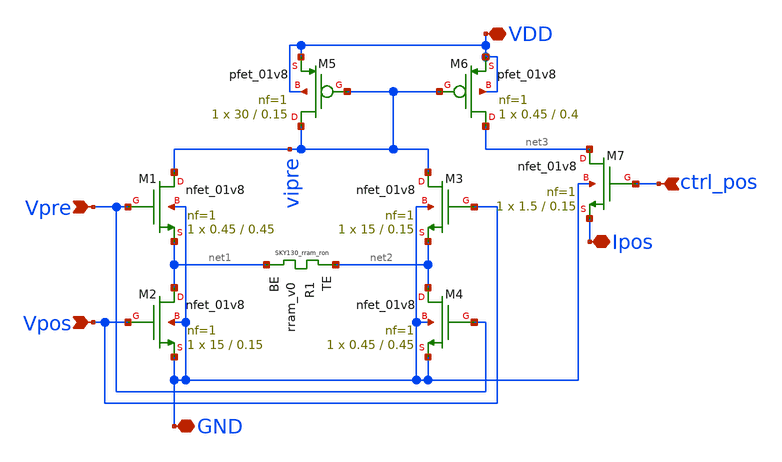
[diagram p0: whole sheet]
** sch_path: SNN/Syn_7T1R.sch
**.subckt Syn_7T1R Vpre Vpos GND Ipos VDD ctrl_pos
*.ipin Vpre
*.ipin Vpos
*.iopin GND
*.iopin Ipos
*.iopin VDD
*.ipin ctrl_pos
XM1 vipre Vpre net1 GND sky130_fd_pr__nfet_01v8 L=0.45 W=0.45 nf=1 ad='int((nf+1)/2) * W/nf * 0.29' as='int((nf+2)/2) * W/nf * 0.29'
+ pd='2*int((nf+1)/2) * (W/nf + 0.29)' ps='2*int((nf+2)/2) * (W/nf + 0.29)' nrd='0.29 / W' nrs='0.29 / W'
+ sa=0 sb=0 sd=0 mult=1 m=1
XR1 net2 net1 rram_v0
XM3 vipre Vpos net2 GND sky130_fd_pr__nfet_01v8 L=0.15 W=15 nf=1 ad='int((nf+1)/2) * W/nf * 0.29' as='int((nf+2)/2) * W/nf * 0.29'
+ pd='2*int((nf+1)/2) * (W/nf + 0.29)' ps='2*int((nf+2)/2) * (W/nf + 0.29)' nrd='0.29 / W' nrs='0.29 / W'
+ sa=0 sb=0 sd=0 mult=1 m=1
XM6 net3 vipre VDD VDD sky130_fd_pr__pfet_01v8 L=0.4 W=0.45 nf=1 ad='int((nf+1)/2) * W/nf * 0.29' as='int((nf+2)/2) * W/nf * 0.29'
+ pd='2*int((nf+1)/2) * (W/nf + 0.29)' ps='2*int((nf+2)/2) * (W/nf + 0.29)' nrd='0.29 / W' nrs='0.29 / W'
+ sa=0 sb=0 sd=0 mult=1 m=1
XM5 vipre vipre VDD VDD sky130_fd_pr__pfet_01v8 L=0.15 W=30 nf=1 ad='int((nf+1)/2) * W/nf * 0.29' as='int((nf+2)/2) * W/nf * 0.29'
+ pd='2*int((nf+1)/2) * (W/nf + 0.29)' ps='2*int((nf+2)/2) * (W/nf + 0.29)' nrd='0.29 / W' nrs='0.29 / W'
+ sa=0 sb=0 sd=0 mult=1 m=1
XM2 net1 Vpos GND GND sky130_fd_pr__nfet_01v8 L=0.15 W=15 nf=1 ad='int((nf+1)/2) * W/nf * 0.29' as='int((nf+2)/2) * W/nf * 0.29'
+ pd='2*int((nf+1)/2) * (W/nf + 0.29)' ps='2*int((nf+2)/2) * (W/nf + 0.29)' nrd='0.29 / W' nrs='0.29 / W'
+ sa=0 sb=0 sd=0 mult=1 m=1
XM4 net2 Vpre GND GND sky130_fd_pr__nfet_01v8 L=0.45 W=0.45 nf=1 ad='int((nf+1)/2) * W/nf * 0.29' as='int((nf+2)/2) * W/nf * 0.29'
+ pd='2*int((nf+1)/2) * (W/nf + 0.29)' ps='2*int((nf+2)/2) * (W/nf + 0.29)' nrd='0.29 / W' nrs='0.29 / W'
+ sa=0 sb=0 sd=0 mult=1 m=1
XM7 net3 ctrl_pos Ipos GND sky130_fd_pr__nfet_01v8 L=0.15 W=1.5 nf=1 ad='int((nf+1)/2) * W/nf * 0.29'
+ as='int((nf+2)/2) * W/nf * 0.29' pd='2*int((nf+1)/2) * (W/nf + 0.29)' ps='2*int((nf+2)/2) * (W/nf + 0.29)'
+ nrd='0.29 / W' nrs='0.29 / W' sa=0 sb=0 sd=0 mult=1 m=1
**.ends
.end
